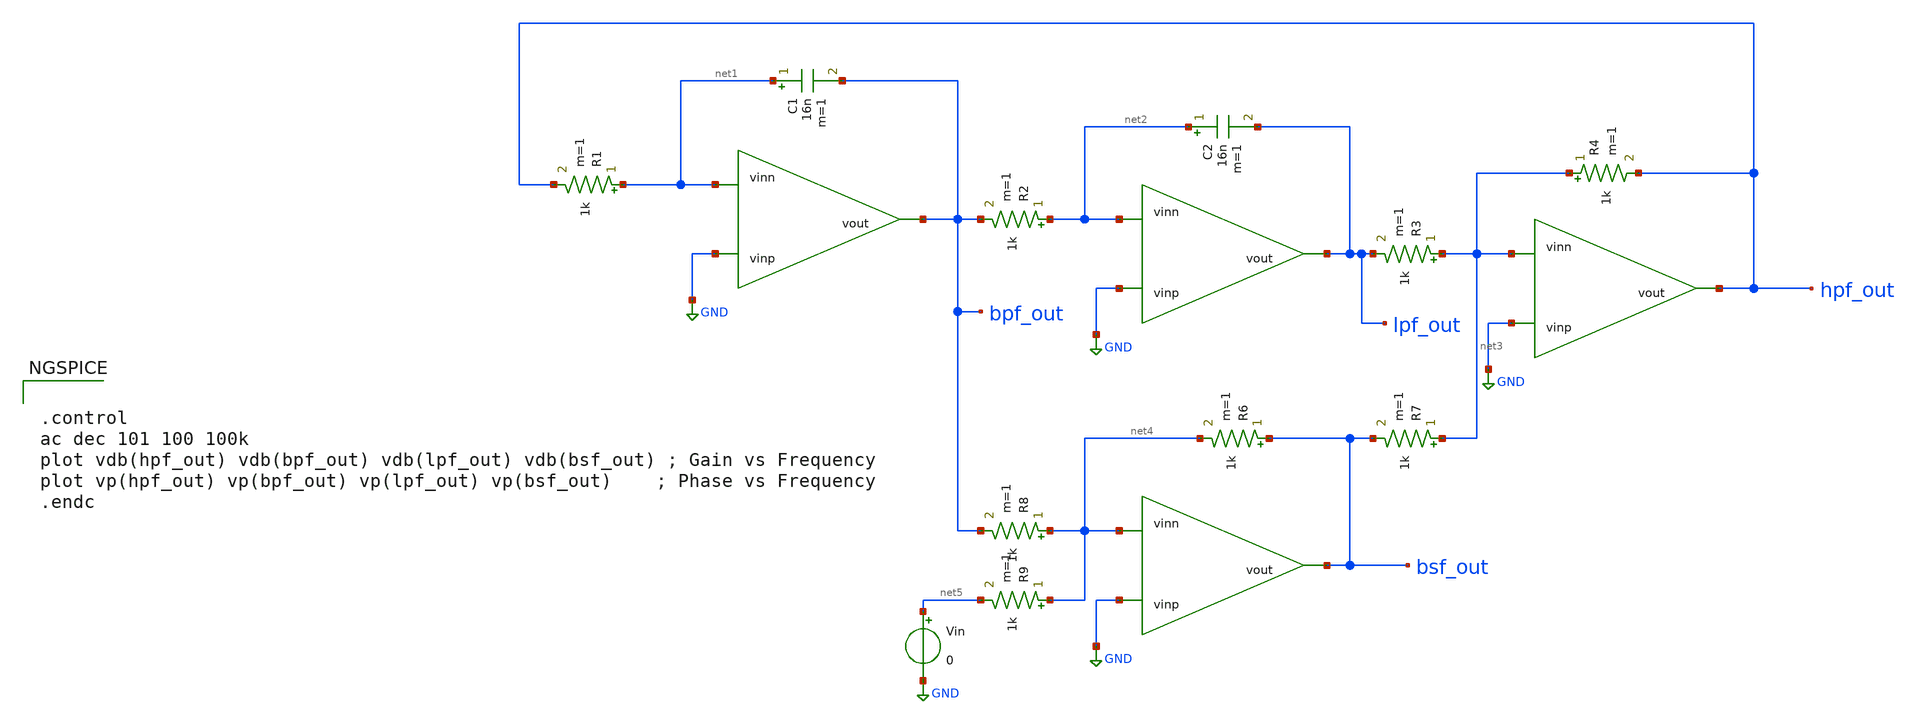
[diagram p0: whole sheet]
** sch_path: 2_Ideal_Cir/toplevel.sch
**.subckt toplevel
R1 net1 hpf_out 1k m=1
C1 net1 bpf_out 16n m=1
R2 net2 bpf_out 1k m=1
C2 net2 lpf_out 16n m=1
R3 net3 lpf_out 1k m=1
R4 net3 hpf_out 1k m=1
R6 bsf_out net4 1k m=1
R7 net3 bsf_out 1k m=1
R8 net4 bpf_out 1k m=1
R9 net4 net5 1k m=1
Vin net5 GND 0
**** begin user architecture code


.control
ac dec 101 100 100k
plot vdb(hpf_out) vdb(bpf_out) vdb(lpf_out) vdb(bsf_out) ; Gain vs Frequency
plot vp(hpf_out) vp(bpf_out) vp(lpf_out) vp(bsf_out)    ; Phase vs Frequency
.endc


**** end user architecture code
**.ends
.GLOBAL GND
.end
